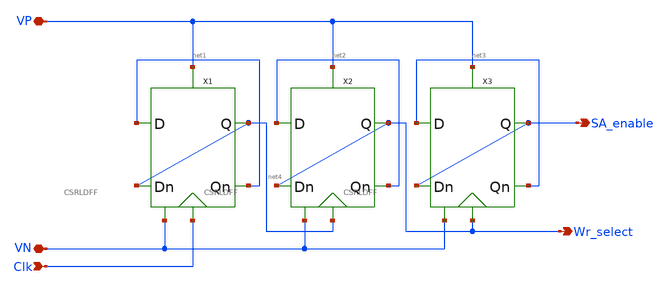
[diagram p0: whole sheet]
** sch_path: DRAM_Components/Schematic/CounterRefresh.sch
**.subckt CounterRefresh VP VN Clk SA_enable Wr_select
*.iopin VP
*.iopin VN
*.ipin Clk
*.opin SA_enable
*.opin Wr_select
X1 net1 Clk VN VP net1 net4 net4 CSRLDFF
X2 net2 net4 VN VP net2 Wr_select Wr_select CSRLDFF
X3 net3 Wr_select VN VP net3 SA_enable SA_enable CSRLDFF
**.ends

* expanding   symbol:  /home/madvlsi/Desktop/CMOSDRAM/DRAM_Components/Schematic/CSRLDFF.sym # of
*+ pins=7
** sym_path: DRAM_Components/Schematic/CSRLDFF.sym
** sch_path: DRAM_Components/Schematic/CSRLDFF.sch
.subckt CSRLDFF D clk VN VP Qn Q Dn
*.ipin D
*.ipin clk
*.iopin VN
*.opin Q
*.opin Qn
*.ipin Dn
*.iopin VP
XM1 net3 clk D VP sky130_fd_pr__pfet_01v8 L=0.6 W=1 nf=1 ad='int((nf+1)/2) * W/nf * 0.29' as='int((nf+2)/2) * W/nf * 0.29'
+ pd='2*int((nf+1)/2) * (W/nf + 0.29)' ps='2*int((nf+2)/2) * (W/nf + 0.29)' nrd='0.29 / W' nrs='0.29 / W'
+ sa=0 sb=0 sd=0 mult=1 m=1
XM2 net2 clk Dn VP sky130_fd_pr__pfet_01v8 L=0.6 W=1 nf=1 ad='int((nf+1)/2) * W/nf * 0.29' as='int((nf+2)/2) * W/nf * 0.29'
+ pd='2*int((nf+1)/2) * (W/nf + 0.29)' ps='2*int((nf+2)/2) * (W/nf + 0.29)' nrd='0.29 / W' nrs='0.29 / W'
+ sa=0 sb=0 sd=0 mult=1 m=1
XM3 net3 clk Q VN sky130_fd_pr__nfet_01v8 L=0.6 W=1 nf=1 ad='int((nf+1)/2) * W/nf * 0.29' as='int((nf+2)/2) * W/nf * 0.29'
+ pd='2*int((nf+1)/2) * (W/nf + 0.29)' ps='2*int((nf+2)/2) * (W/nf + 0.29)' nrd='0.29 / W' nrs='0.29 / W'
+ sa=0 sb=0 sd=0 mult=1 m=1
XM4 net2 clk Qn VN sky130_fd_pr__nfet_01v8 L=0.6 W=1 nf=1 ad='int((nf+1)/2) * W/nf * 0.29' as='int((nf+2)/2) * W/nf * 0.29'
+ pd='2*int((nf+1)/2) * (W/nf + 0.29)' ps='2*int((nf+2)/2) * (W/nf + 0.29)' nrd='0.29 / W' nrs='0.29 / W'
+ sa=0 sb=0 sd=0 mult=1 m=1
XM5 net1 clk VN VN sky130_fd_pr__nfet_01v8 L=0.15 W=1 nf=1 ad='int((nf+1)/2) * W/nf * 0.29' as='int((nf+2)/2) * W/nf * 0.29'
+ pd='2*int((nf+1)/2) * (W/nf + 0.29)' ps='2*int((nf+2)/2) * (W/nf + 0.29)' nrd='0.29 / W' nrs='0.29 / W'
+ sa=0 sb=0 sd=0 mult=1 m=1
XM6 net2 net3 net1 VN sky130_fd_pr__nfet_01v8 L=0.15 W=1 nf=1 ad='int((nf+1)/2) * W/nf * 0.29' as='int((nf+2)/2) * W/nf * 0.29'
+ pd='2*int((nf+1)/2) * (W/nf + 0.29)' ps='2*int((nf+2)/2) * (W/nf + 0.29)' nrd='0.29 / W' nrs='0.29 / W'
+ sa=0 sb=0 sd=0 mult=1 m=1
XM7 net3 net2 net1 VN sky130_fd_pr__nfet_01v8 L=0.15 W=1 nf=1 ad='int((nf+1)/2) * W/nf * 0.29' as='int((nf+2)/2) * W/nf * 0.29'
+ pd='2*int((nf+1)/2) * (W/nf + 0.29)' ps='2*int((nf+2)/2) * (W/nf + 0.29)' nrd='0.29 / W' nrs='0.29 / W'
+ sa=0 sb=0 sd=0 mult=1 m=1
XM8 net2 net3 VP VP sky130_fd_pr__pfet_01v8 L=0.15 W=1 nf=1 ad='int((nf+1)/2) * W/nf * 0.29' as='int((nf+2)/2) * W/nf * 0.29'
+ pd='2*int((nf+1)/2) * (W/nf + 0.29)' ps='2*int((nf+2)/2) * (W/nf + 0.29)' nrd='0.29 / W' nrs='0.29 / W'
+ sa=0 sb=0 sd=0 mult=1 m=1
XM9 net3 net2 VP VP sky130_fd_pr__pfet_01v8 L=0.15 W=1 nf=1 ad='int((nf+1)/2) * W/nf * 0.29' as='int((nf+2)/2) * W/nf * 0.29'
+ pd='2*int((nf+1)/2) * (W/nf + 0.29)' ps='2*int((nf+2)/2) * (W/nf + 0.29)' nrd='0.29 / W' nrs='0.29 / W'
+ sa=0 sb=0 sd=0 mult=1 m=1
XM10 net4 clk VP VP sky130_fd_pr__pfet_01v8 L=0.15 W=1 nf=1 ad='int((nf+1)/2) * W/nf * 0.29' as='int((nf+2)/2) * W/nf * 0.29'
+ pd='2*int((nf+1)/2) * (W/nf + 0.29)' ps='2*int((nf+2)/2) * (W/nf + 0.29)' nrd='0.29 / W' nrs='0.29 / W'
+ sa=0 sb=0 sd=0 mult=1 m=1
XM11 Qn Q net4 VP sky130_fd_pr__pfet_01v8 L=0.15 W=1 nf=1 ad='int((nf+1)/2) * W/nf * 0.29' as='int((nf+2)/2) * W/nf * 0.29'
+ pd='2*int((nf+1)/2) * (W/nf + 0.29)' ps='2*int((nf+2)/2) * (W/nf + 0.29)' nrd='0.29 / W' nrs='0.29 / W'
+ sa=0 sb=0 sd=0 mult=1 m=1
XM12 Q Qn net4 VP sky130_fd_pr__pfet_01v8 L=0.15 W=1 nf=1 ad='int((nf+1)/2) * W/nf * 0.29' as='int((nf+2)/2) * W/nf * 0.29'
+ pd='2*int((nf+1)/2) * (W/nf + 0.29)' ps='2*int((nf+2)/2) * (W/nf + 0.29)' nrd='0.29 / W' nrs='0.29 / W'
+ sa=0 sb=0 sd=0 mult=1 m=1
XM13 Qn Q VN VN sky130_fd_pr__nfet_01v8 L=0.15 W=1 nf=1 ad='int((nf+1)/2) * W/nf * 0.29' as='int((nf+2)/2) * W/nf * 0.29'
+ pd='2*int((nf+1)/2) * (W/nf + 0.29)' ps='2*int((nf+2)/2) * (W/nf + 0.29)' nrd='0.29 / W' nrs='0.29 / W'
+ sa=0 sb=0 sd=0 mult=1 m=1
XM14 Q Qn VN VN sky130_fd_pr__nfet_01v8 L=0.15 W=1 nf=1 ad='int((nf+1)/2) * W/nf * 0.29' as='int((nf+2)/2) * W/nf * 0.29'
+ pd='2*int((nf+1)/2) * (W/nf + 0.29)' ps='2*int((nf+2)/2) * (W/nf + 0.29)' nrd='0.29 / W' nrs='0.29 / W'
+ sa=0 sb=0 sd=0 mult=1 m=1
.ends

.end
